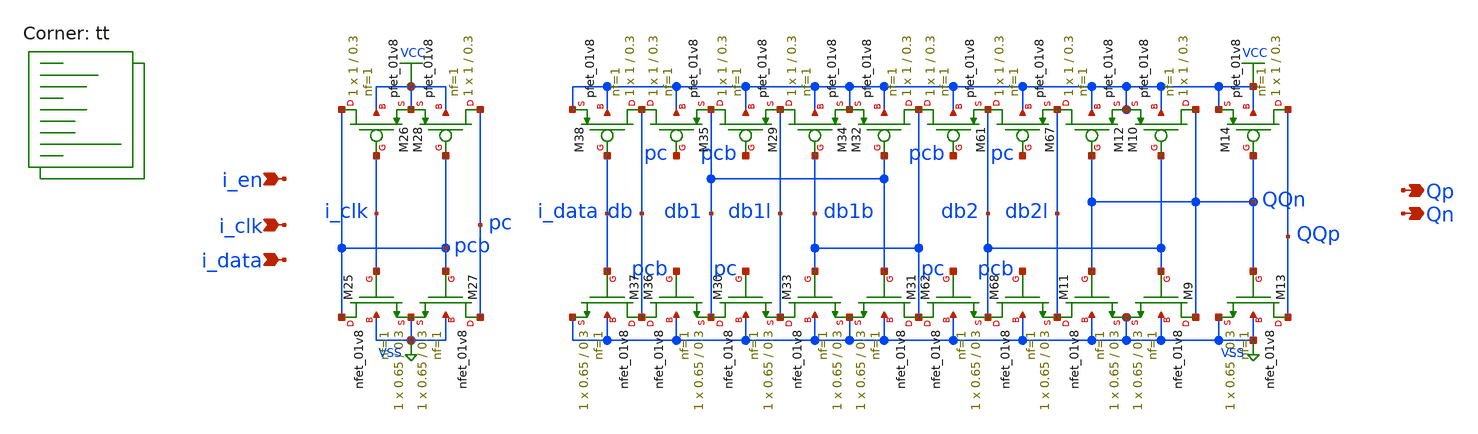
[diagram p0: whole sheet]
** sch_path: elements/edffe.sch
**.subckt edffe i_clk i_data i_en Qp Qn
*.ipin i_clk
*.ipin i_data
*.ipin i_en
*.opin Qp
*.opin Qn
XM25 pcb i_clk VSS VSS sky130_fd_pr__nfet_01v8 L=0.3 W=0.65 nf=1 ad='int((1 + 1)/2) * 0.65 / 1 * 0.29'
+ as='int((1 + 2)/2) * 0.65 / 1 * 0.29' pd='2*int((1 + 1)/2) * (0.65 / 1 + 0.29)' ps='2*int((1 + 2)/2) * (0.65 / 1 + 0.29)'
+ nrd='0.29 / 0.65 ' nrs='0.29 / 0.65 ' sa=0 sb=0 sd=0 mult=1 m=1
XM26 pcb i_clk VCC VCC sky130_fd_pr__pfet_01v8 L=0.3 W=1 nf=1 ad='int((nf+1)/2) * W/nf * 0.29' as='int((nf+2)/2) * W/nf * 0.29'
+ pd='2*int((nf+1)/2) * (W/nf + 0.29)' ps='2*int((nf+2)/2) * (W/nf + 0.29)' nrd='0.29 / W' nrs='0.29 / W'
+ sa=0 sb=0 sd=0 mult=1 m=1
XM27 pc pcb VSS VSS sky130_fd_pr__nfet_01v8 L=0.3 W=0.65 nf=1 ad='int((1 + 1)/2) * 0.65 / 1 * 0.29' as='int((1 + 2)/2) * 0.65 / 1 * 0.29'
+ pd='2*int((1 + 1)/2) * (0.65 / 1 + 0.29)' ps='2*int((1 + 2)/2) * (0.65 / 1 + 0.29)' nrd='0.29 / 0.65 '
+ nrs='0.29 / 0.65 ' sa=0 sb=0 sd=0 mult=1 m=1
XM28 pc pcb VCC VCC sky130_fd_pr__pfet_01v8 L=0.3 W=1 nf=1 ad='int((nf+1)/2) * W/nf * 0.29' as='int((nf+2)/2) * W/nf * 0.29'
+ pd='2*int((nf+1)/2) * (W/nf + 0.29)' ps='2*int((nf+2)/2) * (W/nf + 0.29)' nrd='0.29 / W' nrs='0.29 / W'
+ sa=0 sb=0 sd=0 mult=1 m=1
XM29 db1 pcb db1l VCC sky130_fd_pr__pfet_01v8 L=0.3 W=1 nf=1 ad='int((nf+1)/2) * W/nf * 0.29' as='int((nf+2)/2) * W/nf * 0.29'
+ pd='2*int((nf+1)/2) * (W/nf + 0.29)' ps='2*int((nf+2)/2) * (W/nf + 0.29)' nrd='0.29 / W' nrs='0.29 / W'
+ sa=0 sb=0 sd=0 mult=1 m=1
XM30 db1 pc db1l VSS sky130_fd_pr__nfet_01v8 L=0.3 W=0.65 nf=1 ad='int((1 + 1)/2) * 0.65 / 1 * 0.29'
+ as='int((1 + 2)/2) * 0.65 / 1 * 0.29' pd='2*int((1 + 1)/2) * (0.65 / 1 + 0.29)' ps='2*int((1 + 2)/2) * (0.65 / 1 + 0.29)'
+ nrd='0.29 / 0.65 ' nrs='0.29 / 0.65 ' sa=0 sb=0 sd=0 mult=1 m=1
XM31 db1b db1 VSS VSS sky130_fd_pr__nfet_01v8 L=0.3 W=0.65 nf=1 ad='int((1 + 1)/2) * 0.65 / 1 * 0.29'
+ as='int((1 + 2)/2) * 0.65 / 1 * 0.29' pd='2*int((1 + 1)/2) * (0.65 / 1 + 0.29)' ps='2*int((1 + 2)/2) * (0.65 / 1 + 0.29)'
+ nrd='0.29 / 0.65 ' nrs='0.29 / 0.65 ' sa=0 sb=0 sd=0 mult=1 m=1
XM32 db1b db1 VCC VCC sky130_fd_pr__pfet_01v8 L=0.3 W=1 nf=1 ad='int((nf+1)/2) * W/nf * 0.29' as='int((nf+2)/2) * W/nf * 0.29'
+ pd='2*int((nf+1)/2) * (W/nf + 0.29)' ps='2*int((nf+2)/2) * (W/nf + 0.29)' nrd='0.29 / W' nrs='0.29 / W'
+ sa=0 sb=0 sd=0 mult=1 m=1
XM33 db1l db1b VSS VSS sky130_fd_pr__nfet_01v8 L=0.3 W=0.65 nf=1 ad='int((1 + 1)/2) * 0.65 / 1 * 0.29'
+ as='int((1 + 2)/2) * 0.65 / 1 * 0.29' pd='2*int((1 + 1)/2) * (0.65 / 1 + 0.29)' ps='2*int((1 + 2)/2) * (0.65 / 1 + 0.29)'
+ nrd='0.29 / 0.65 ' nrs='0.29 / 0.65 ' sa=0 sb=0 sd=0 mult=1 m=1
XM34 db1l db1b VCC VCC sky130_fd_pr__pfet_01v8 L=0.3 W=1 nf=1 ad='int((nf+1)/2) * W/nf * 0.29' as='int((nf+2)/2) * W/nf * 0.29'
+ pd='2*int((nf+1)/2) * (W/nf + 0.29)' ps='2*int((nf+2)/2) * (W/nf + 0.29)' nrd='0.29 / W' nrs='0.29 / W'
+ sa=0 sb=0 sd=0 mult=1 m=1
XM35 db pc db1 VCC sky130_fd_pr__pfet_01v8 L=0.3 W=1 nf=1 ad='int((nf+1)/2) * W/nf * 0.29' as='int((nf+2)/2) * W/nf * 0.29'
+ pd='2*int((nf+1)/2) * (W/nf + 0.29)' ps='2*int((nf+2)/2) * (W/nf + 0.29)' nrd='0.29 / W' nrs='0.29 / W'
+ sa=0 sb=0 sd=0 mult=1 m=1
XM36 db pcb db1 VSS sky130_fd_pr__nfet_01v8 L=0.3 W=0.65 nf=1 ad='int((1 + 1)/2) * 0.65 / 1 * 0.29' as='int((1 + 2)/2) * 0.65 / 1 * 0.29'
+ pd='2*int((1 + 1)/2) * (0.65 / 1 + 0.29)' ps='2*int((1 + 2)/2) * (0.65 / 1 + 0.29)' nrd='0.29 / 0.65 '
+ nrs='0.29 / 0.65 ' sa=0 sb=0 sd=0 mult=1 m=1
XM37 db i_data VSS VSS sky130_fd_pr__nfet_01v8 L=0.3 W=0.65 nf=1 ad='int((1 + 1)/2) * 0.65 / 1 * 0.29'
+ as='int((1 + 2)/2) * 0.65 / 1 * 0.29' pd='2*int((1 + 1)/2) * (0.65 / 1 + 0.29)' ps='2*int((1 + 2)/2) * (0.65 / 1 + 0.29)'
+ nrd='0.29 / 0.65 ' nrs='0.29 / 0.65 ' sa=0 sb=0 sd=0 mult=1 m=1
XM38 db i_data VCC VCC sky130_fd_pr__pfet_01v8 L=0.3 W=1 nf=1 ad='int((nf+1)/2) * W/nf * 0.29' as='int((nf+2)/2) * W/nf * 0.29'
+ pd='2*int((nf+1)/2) * (W/nf + 0.29)' ps='2*int((nf+2)/2) * (W/nf + 0.29)' nrd='0.29 / W' nrs='0.29 / W'
+ sa=0 sb=0 sd=0 mult=1 m=1
XM61 db1b pcb db2 VCC sky130_fd_pr__pfet_01v8 L=0.3 W=1 nf=1 ad='int((nf+1)/2) * W/nf * 0.29' as='int((nf+2)/2) * W/nf * 0.29'
+ pd='2*int((nf+1)/2) * (W/nf + 0.29)' ps='2*int((nf+2)/2) * (W/nf + 0.29)' nrd='0.29 / W' nrs='0.29 / W'
+ sa=0 sb=0 sd=0 mult=1 m=1
XM62 db1b pc db2 VSS sky130_fd_pr__nfet_01v8 L=0.3 W=0.65 nf=1 ad='int((1 + 1)/2) * 0.65 / 1 * 0.29'
+ as='int((1 + 2)/2) * 0.65 / 1 * 0.29' pd='2*int((1 + 1)/2) * (0.65 / 1 + 0.29)' ps='2*int((1 + 2)/2) * (0.65 / 1 + 0.29)'
+ nrd='0.29 / 0.65 ' nrs='0.29 / 0.65 ' sa=0 sb=0 sd=0 mult=1 m=1
XM67 db2 pc db2l VCC sky130_fd_pr__pfet_01v8 L=0.3 W=1 nf=1 ad='int((nf+1)/2) * W/nf * 0.29' as='int((nf+2)/2) * W/nf * 0.29'
+ pd='2*int((nf+1)/2) * (W/nf + 0.29)' ps='2*int((nf+2)/2) * (W/nf + 0.29)' nrd='0.29 / W' nrs='0.29 / W'
+ sa=0 sb=0 sd=0 mult=1 m=1
XM68 db2 pcb db2l VSS sky130_fd_pr__nfet_01v8 L=0.3 W=0.65 nf=1 ad='int((1 + 1)/2) * 0.65 / 1 * 0.29'
+ as='int((1 + 2)/2) * 0.65 / 1 * 0.29' pd='2*int((1 + 1)/2) * (0.65 / 1 + 0.29)' ps='2*int((1 + 2)/2) * (0.65 / 1 + 0.29)'
+ nrd='0.29 / 0.65 ' nrs='0.29 / 0.65 ' sa=0 sb=0 sd=0 mult=1 m=1
XM9 QQn db2 VSS VSS sky130_fd_pr__nfet_01v8 L=0.3 W=0.65 nf=1 ad='int((1 + 1)/2) * 0.65 / 1 * 0.29' as='int((1 + 2)/2) * 0.65 / 1 * 0.29'
+ pd='2*int((1 + 1)/2) * (0.65 / 1 + 0.29)' ps='2*int((1 + 2)/2) * (0.65 / 1 + 0.29)' nrd='0.29 / 0.65 '
+ nrs='0.29 / 0.65 ' sa=0 sb=0 sd=0 mult=1 m=1
XM10 QQn db2 VCC VCC sky130_fd_pr__pfet_01v8 L=0.3 W=1 nf=1 ad='int((nf+1)/2) * W/nf * 0.29' as='int((nf+2)/2) * W/nf * 0.29'
+ pd='2*int((nf+1)/2) * (W/nf + 0.29)' ps='2*int((nf+2)/2) * (W/nf + 0.29)' nrd='0.29 / W' nrs='0.29 / W'
+ sa=0 sb=0 sd=0 mult=1 m=1
XM11 db2l QQn VSS VSS sky130_fd_pr__nfet_01v8 L=0.3 W=0.65 nf=1 ad='int((1 + 1)/2) * 0.65 / 1 * 0.29'
+ as='int((1 + 2)/2) * 0.65 / 1 * 0.29' pd='2*int((1 + 1)/2) * (0.65 / 1 + 0.29)' ps='2*int((1 + 2)/2) * (0.65 / 1 + 0.29)'
+ nrd='0.29 / 0.65 ' nrs='0.29 / 0.65 ' sa=0 sb=0 sd=0 mult=1 m=1
XM12 db2l QQn VCC VCC sky130_fd_pr__pfet_01v8 L=0.3 W=1 nf=1 ad='int((nf+1)/2) * W/nf * 0.29' as='int((nf+2)/2) * W/nf * 0.29'
+ pd='2*int((nf+1)/2) * (W/nf + 0.29)' ps='2*int((nf+2)/2) * (W/nf + 0.29)' nrd='0.29 / W' nrs='0.29 / W'
+ sa=0 sb=0 sd=0 mult=1 m=1
XM13 QQp QQn VSS VSS sky130_fd_pr__nfet_01v8 L=0.3 W=0.65 nf=1 ad='int((1 + 1)/2) * 0.65 / 1 * 0.29'
+ as='int((1 + 2)/2) * 0.65 / 1 * 0.29' pd='2*int((1 + 1)/2) * (0.65 / 1 + 0.29)' ps='2*int((1 + 2)/2) * (0.65 / 1 + 0.29)'
+ nrd='0.29 / 0.65 ' nrs='0.29 / 0.65 ' sa=0 sb=0 sd=0 mult=1 m=1
XM14 QQp QQn VCC VCC sky130_fd_pr__pfet_01v8 L=0.3 W=1 nf=1 ad='int((nf+1)/2) * W/nf * 0.29' as='int((nf+2)/2) * W/nf * 0.29'
+ pd='2*int((nf+1)/2) * (W/nf + 0.29)' ps='2*int((nf+2)/2) * (W/nf + 0.29)' nrd='0.29 / W' nrs='0.29 / W'
+ sa=0 sb=0 sd=0 mult=1 m=1
**** begin user architecture code
.lib $::SKYWATER_MODELS/sky130.lib.spice tt

.include $::SKYWATER_STDCELLS/sky130_fd_sc_hd.spice




*.option method=gear
.param VCC=1.8

.include stimuli_edffe.cir
.control
* save all
tran 0.1n 40n uic
write edffe.raw
acct
rusage
.endc






**** end user architecture code
**.ends
.GLOBAL VCC
.GLOBAL VSS
.end
